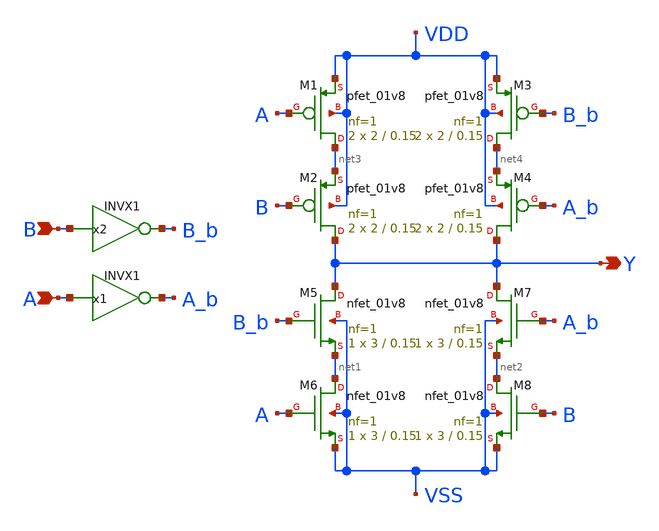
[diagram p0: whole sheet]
** sch_path: lib/xschem/XNOR2X1.sch
**.subckt XNOR2X1 Y A B
*.opin Y
*.ipin A
*.ipin B
x1 A_b A VDD VSS INVX1
x2 B_b B VDD VSS INVX1
XM1 net3 A VDD VDD sky130_fd_pr__pfet_01v8 L=0.15 W=2 nf=1 ad='int((nf+1)/2) * W/nf * 0.29' as='int((nf+2)/2) * W/nf * 0.29'
+ pd='2*int((nf+1)/2) * (W/nf + 0.29)' ps='2*int((nf+2)/2) * (W/nf + 0.29)' nrd='0.29 / W' nrs='0.29 / W'
+ sa=0 sb=0 sd=0 mult=2 m=2
XM2 Y B net3 VDD sky130_fd_pr__pfet_01v8 L=0.15 W=2 nf=1 ad='int((nf+1)/2) * W/nf * 0.29' as='int((nf+2)/2) * W/nf * 0.29'
+ pd='2*int((nf+1)/2) * (W/nf + 0.29)' ps='2*int((nf+2)/2) * (W/nf + 0.29)' nrd='0.29 / W' nrs='0.29 / W'
+ sa=0 sb=0 sd=0 mult=2 m=2
XM3 net4 B_b VDD VDD sky130_fd_pr__pfet_01v8 L=0.15 W=2 nf=1 ad='int((nf+1)/2) * W/nf * 0.29' as='int((nf+2)/2) * W/nf * 0.29'
+ pd='2*int((nf+1)/2) * (W/nf + 0.29)' ps='2*int((nf+2)/2) * (W/nf + 0.29)' nrd='0.29 / W' nrs='0.29 / W'
+ sa=0 sb=0 sd=0 mult=2 m=2
XM4 Y A_b net4 VDD sky130_fd_pr__pfet_01v8 L=0.15 W=2 nf=1 ad='int((nf+1)/2) * W/nf * 0.29' as='int((nf+2)/2) * W/nf * 0.29'
+ pd='2*int((nf+1)/2) * (W/nf + 0.29)' ps='2*int((nf+2)/2) * (W/nf + 0.29)' nrd='0.29 / W' nrs='0.29 / W'
+ sa=0 sb=0 sd=0 mult=2 m=2
XM5 Y B_b net1 VSS sky130_fd_pr__nfet_01v8 L=0.15 W=3 nf=1 ad='int((nf+1)/2) * W/nf * 0.29' as='int((nf+2)/2) * W/nf * 0.29'
+ pd='2*int((nf+1)/2) * (W/nf + 0.29)' ps='2*int((nf+2)/2) * (W/nf + 0.29)' nrd='0.29 / W' nrs='0.29 / W'
+ sa=0 sb=0 sd=0 mult=1 m=1
XM6 net1 A VSS VSS sky130_fd_pr__nfet_01v8 L=0.15 W=3 nf=1 ad='int((nf+1)/2) * W/nf * 0.29' as='int((nf+2)/2) * W/nf * 0.29'
+ pd='2*int((nf+1)/2) * (W/nf + 0.29)' ps='2*int((nf+2)/2) * (W/nf + 0.29)' nrd='0.29 / W' nrs='0.29 / W'
+ sa=0 sb=0 sd=0 mult=1 m=1
XM7 Y A_b net2 VSS sky130_fd_pr__nfet_01v8 L=0.15 W=3 nf=1 ad='int((nf+1)/2) * W/nf * 0.29' as='int((nf+2)/2) * W/nf * 0.29'
+ pd='2*int((nf+1)/2) * (W/nf + 0.29)' ps='2*int((nf+2)/2) * (W/nf + 0.29)' nrd='0.29 / W' nrs='0.29 / W'
+ sa=0 sb=0 sd=0 mult=1 m=1
XM8 net2 B VSS VSS sky130_fd_pr__nfet_01v8 L=0.15 W=3 nf=1 ad='int((nf+1)/2) * W/nf * 0.29' as='int((nf+2)/2) * W/nf * 0.29'
+ pd='2*int((nf+1)/2) * (W/nf + 0.29)' ps='2*int((nf+2)/2) * (W/nf + 0.29)' nrd='0.29 / W' nrs='0.29 / W'
+ sa=0 sb=0 sd=0 mult=1 m=1
**.ends

* expanding   symbol:  INVX1.sym # of pins=2
** sym_path: archives/lib/xschem/INVX1.sym
** sch_path: archives/lib/xschem/INVX1.sch
.subckt INVX1 Y A VDD VSS
*.opin Y
*.ipin A
XM1 Y A VSS VSS sky130_fd_pr__nfet_01v8 L=0.15 W=3 nf=1 ad='int((nf+1)/2) * W/nf * 0.29' as='int((nf+2)/2) * W/nf * 0.29'
+ pd='2*int((nf+1)/2) * (W/nf + 0.29)' ps='2*int((nf+2)/2) * (W/nf + 0.29)' nrd='0.29 / W' nrs='0.29 / W'
+ sa=0 sb=0 sd=0 mult=1 m=1
XM2 Y A VDD VDD sky130_fd_pr__pfet_01v8 L=0.15 W=2 nf=1 ad='int((nf+1)/2) * W/nf * 0.29' as='int((nf+2)/2) * W/nf * 0.29'
+ pd='2*int((nf+1)/2) * (W/nf + 0.29)' ps='2*int((nf+2)/2) * (W/nf + 0.29)' nrd='0.29 / W' nrs='0.29 / W'
+ sa=0 sb=0 sd=0 mult=2 m=2
.ends

.end
